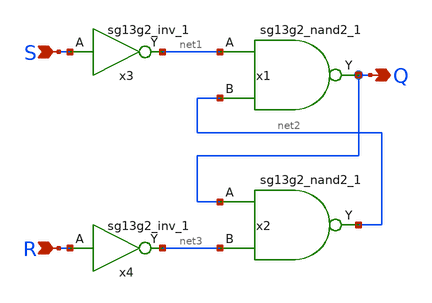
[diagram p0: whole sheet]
** sch_path: 3_real_circuits/sr_latch.sch
**.subckt sr_latch S R Q
*.ipin S
*.ipin R
*.opin Q
x1 Q net1 net2 VDD VSS sg13g2_nand2_1
x2 net2 Q net3 VDD VSS sg13g2_nand2_1
x3 net1 S VDD VSS sg13g2_inv_1
x4 net3 R VDD VSS sg13g2_inv_1
**.ends

* expanding   symbol:  sg13g2_stdcells/sg13g2_nand2_1.sym # of pins=3
** sym_path: sg13g2_stdcells/sg13g2_nand2_1.sym
** sch_path: sg13g2_stdcells/sg13g2_nand2_1.sch
.subckt sg13g2_nand2_1 Y A B VDD VSS
*.iopin VDD
*.iopin VSS
*.ipin A
*.ipin B
*.opin Y
XM1 Y A net1 VSS sg13_lv_nmos w=740.00n l=130.00n ng=1 m=1 mm_ok=1
XM2 net1 B VSS VSS sg13_lv_nmos w=740.00n l=130.00n ng=1 m=1 mm_ok=1
XM3 Y A VDD VDD sg13_lv_pmos w=1.12u l=130.00n ng=1 m=1 mm_ok=1
XM4 Y B VDD VDD sg13_lv_pmos w=1.12u l=130.00n ng=1 m=1 mm_ok=1
.ends


* expanding   symbol:  sg13g2_stdcells/sg13g2_inv_1.sym # of pins=2
** sym_path: sg13g2_stdcells/sg13g2_inv_1.sym
** sch_path: sg13g2_stdcells/sg13g2_inv_1.sch
.subckt sg13g2_inv_1 Y A VDD VSS
*.opin Y
*.ipin A
*.iopin VDD
*.iopin VSS
XM1 Y A VSS VSS sg13_lv_nmos w=740.00n l=130.00n ng=1 m=1 mm_ok=1
XM2 Y A VDD VDD sg13_lv_pmos w=1.12u l=130.00n ng=1 m=1 mm_ok=1
.ends

.end
